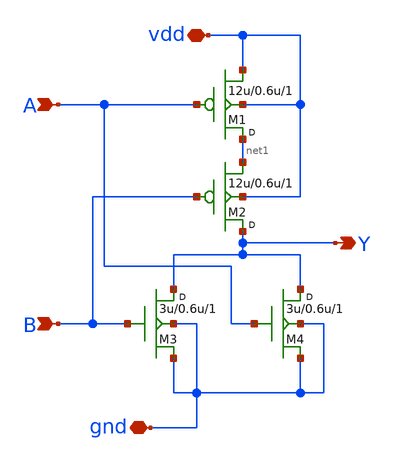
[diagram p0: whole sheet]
** sch_path: lab7/sch/made/NORx.sch
**.subckt NORx A B Y vdd gnd
*.ipin A
*.ipin B
*.opin Y
*.iopin vdd
*.iopin gnd
M1 net1 A vdd vdd pfet w=12u l=0.6u m=1
M2 Y B net1 vdd pfet w=12u l=0.6u m=1
M3 Y B gnd gnd nfet w=3u l=0.6u m=1
M4 Y A gnd gnd nfet w=3u l=0.6u m=1
**.ends
.end
